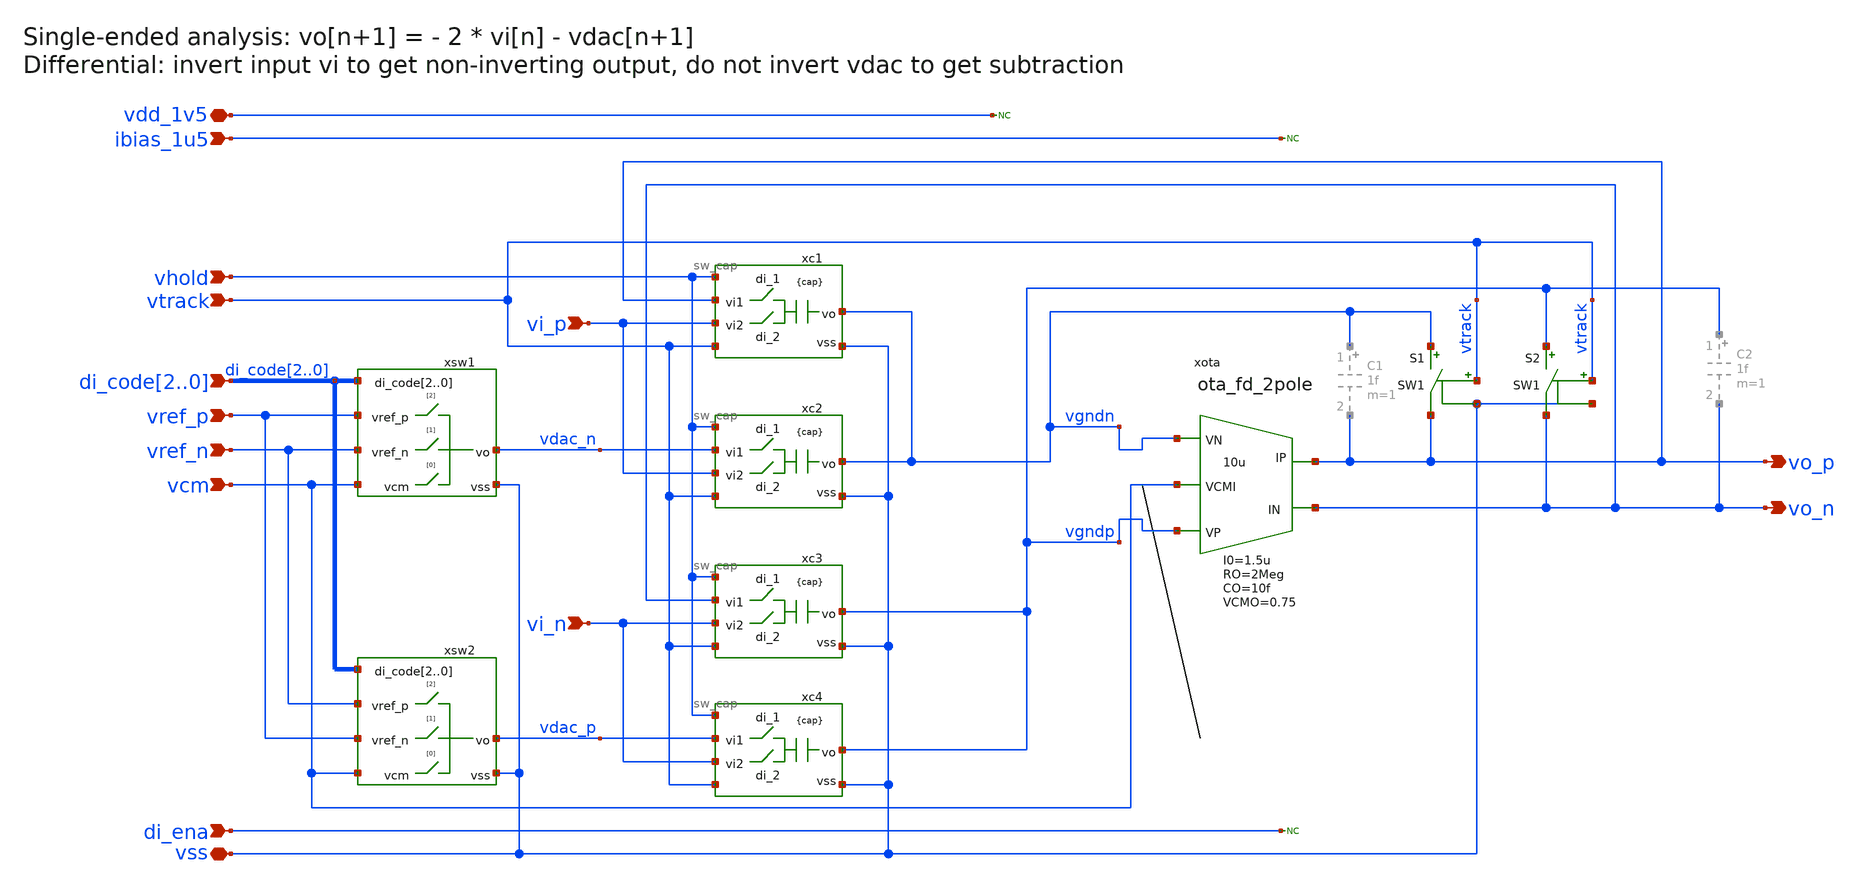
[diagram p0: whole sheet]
** sch_path: xschem/mdac-tri-lvl-ideal.sch
**.subckt mdac-tri-lvl-ideal vi_p vi_n di_ena vss vdd_1v5 ibias_1u5 vo_n vo_p vref_p vref_n vcm
*+ di_code2,di_code1,di_code0 vtrack vhold
*.ipin vi_p
*.ipin vi_n
*.ipin di_ena
*.iopin vss
*.iopin vdd_1v5
*.ipin ibias_1u5
*.opin vo_n
*.opin vo_p
*.ipin vref_p
*.ipin vref_n
*.ipin vcm
*.ipin di_code2,di_code1,di_code0
*.ipin vtrack
*.ipin vhold
S1 vgndn vo_p vtrack vss SW1
S2 vgndp vo_n vtrack vss SW1
xc1 vhold vo_p vgndn vi_p vtrack vss sw_cap cap={cap} ron=1 roff=1G
xc2 vhold vdac_n vgndn vi_p vtrack vss sw_cap cap={cap} ron=1 roff=1G
xc3 vhold vo_n vgndp vi_n vtrack vss sw_cap cap={cap} ron=1 roff=1G
xc4 vhold vdac_p vgndp vi_n vtrack vss sw_cap cap={cap} ron=1 roff=1G
xsw1 di_code2 di_code1 di_code0 vref_p vref_n vdac_n vcm vss sw_dac ron=1 roff=1G
xsw2 di_code2 di_code1 di_code0 vref_n vref_p vdac_p vcm vss sw_dac ron=1 roff=1G
xota vgndn vo_p vo_n vgndp vcm ota_fd_2pole GM=10u RO=2Meg CO=10f RP=1 CP=10f VCMO=0.75 I0=1.5u
* noconn di_ena
* noconn vdd_1v5
* noconn ibias_1u5
**.ends
**** begin user architecture code
.MODEL SW1 SW( VT=0.75 VH=0.01 RON=10 ROFF=100Meg )
**** end user architecture code
.end
